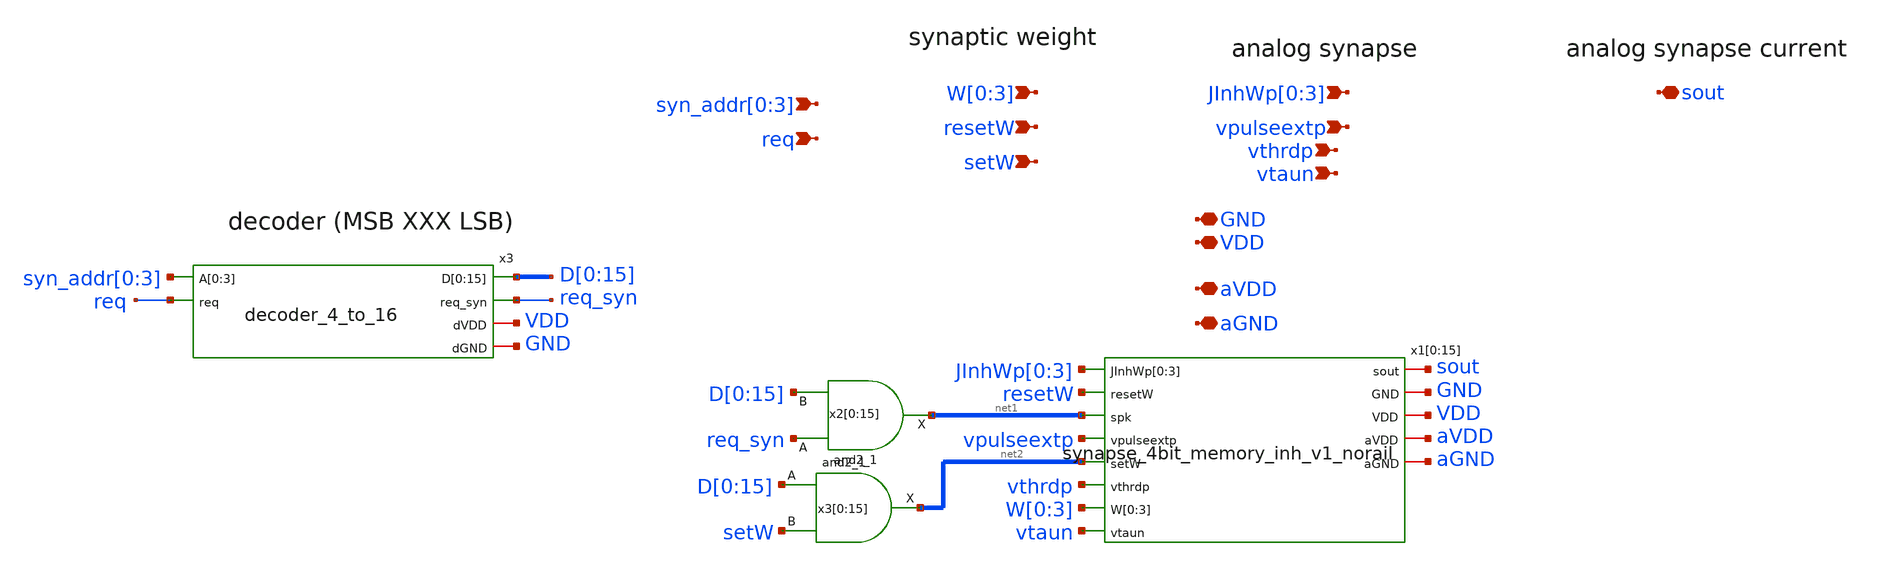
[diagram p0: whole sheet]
** sch_path: design/xschem/synapse_array_programmable_inh_16_to_sout_v1.sch
**.subckt synapse_array_programmable_inh_16_to_sout_v1 vpulseextp
*+ syn_addr[0],syn_addr[1],syn_addr[2],syn_addr[3] W[0],W[1],W[2],W[3] JInhWp[0],JInhWp[1],JInhWp[2],JInhWp[3] sout setW resetW req vthrdp vtaun GND
*+ VDD aVDD aGND
*.ipin vpulseextp
*.ipin syn_addr[0],syn_addr[1],syn_addr[2],syn_addr[3]
*.ipin W[0],W[1],W[2],W[3]
*.ipin JInhWp[0],JInhWp[1],JInhWp[2],JInhWp[3]
*.iopin sout
*.ipin setW
*.ipin resetW
*.ipin req
*.ipin vthrdp
*.ipin vtaun
*.iopin GND
*.iopin VDD
*.iopin aVDD
*.iopin aGND
x3 syn_addr[0] syn_addr[1] syn_addr[2] syn_addr[3] D[0] D[1] D[2] D[3] D[4] D[5] D[6] D[7] D[8] D[9]
+ D[10] D[11] D[12] D[13] D[14] D[15] req req_syn VDD GND decoder_4_to_16
x2[0] req_syn D[0] GND GND VDD VDD net1[15] sky130_fd_sc_hd__and2_1
x2[1] req_syn D[1] GND GND VDD VDD net1[14] sky130_fd_sc_hd__and2_1
x2[2] req_syn D[2] GND GND VDD VDD net1[13] sky130_fd_sc_hd__and2_1
x2[3] req_syn D[3] GND GND VDD VDD net1[12] sky130_fd_sc_hd__and2_1
x2[4] req_syn D[4] GND GND VDD VDD net1[11] sky130_fd_sc_hd__and2_1
x2[5] req_syn D[5] GND GND VDD VDD net1[10] sky130_fd_sc_hd__and2_1
x2[6] req_syn D[6] GND GND VDD VDD net1[9] sky130_fd_sc_hd__and2_1
x2[7] req_syn D[7] GND GND VDD VDD net1[8] sky130_fd_sc_hd__and2_1
x2[8] req_syn D[8] GND GND VDD VDD net1[7] sky130_fd_sc_hd__and2_1
x2[9] req_syn D[9] GND GND VDD VDD net1[6] sky130_fd_sc_hd__and2_1
x2[10] req_syn D[10] GND GND VDD VDD net1[5] sky130_fd_sc_hd__and2_1
x2[11] req_syn D[11] GND GND VDD VDD net1[4] sky130_fd_sc_hd__and2_1
x2[12] req_syn D[12] GND GND VDD VDD net1[3] sky130_fd_sc_hd__and2_1
x2[13] req_syn D[13] GND GND VDD VDD net1[2] sky130_fd_sc_hd__and2_1
x2[14] req_syn D[14] GND GND VDD VDD net1[1] sky130_fd_sc_hd__and2_1
x2[15] req_syn D[15] GND GND VDD VDD net1[0] sky130_fd_sc_hd__and2_1
x3[0] D[0] setW GND GND VDD VDD net2[15] sky130_fd_sc_hd__and2_1
x3[1] D[1] setW GND GND VDD VDD net2[14] sky130_fd_sc_hd__and2_1
x3[2] D[2] setW GND GND VDD VDD net2[13] sky130_fd_sc_hd__and2_1
x3[3] D[3] setW GND GND VDD VDD net2[12] sky130_fd_sc_hd__and2_1
x3[4] D[4] setW GND GND VDD VDD net2[11] sky130_fd_sc_hd__and2_1
x3[5] D[5] setW GND GND VDD VDD net2[10] sky130_fd_sc_hd__and2_1
x3[6] D[6] setW GND GND VDD VDD net2[9] sky130_fd_sc_hd__and2_1
x3[7] D[7] setW GND GND VDD VDD net2[8] sky130_fd_sc_hd__and2_1
x3[8] D[8] setW GND GND VDD VDD net2[7] sky130_fd_sc_hd__and2_1
x3[9] D[9] setW GND GND VDD VDD net2[6] sky130_fd_sc_hd__and2_1
x3[10] D[10] setW GND GND VDD VDD net2[5] sky130_fd_sc_hd__and2_1
x3[11] D[11] setW GND GND VDD VDD net2[4] sky130_fd_sc_hd__and2_1
x3[12] D[12] setW GND GND VDD VDD net2[3] sky130_fd_sc_hd__and2_1
x3[13] D[13] setW GND GND VDD VDD net2[2] sky130_fd_sc_hd__and2_1
x3[14] D[14] setW GND GND VDD VDD net2[1] sky130_fd_sc_hd__and2_1
x3[15] D[15] setW GND GND VDD VDD net2[0] sky130_fd_sc_hd__and2_1
x1[0] sout JInhWp[0] JInhWp[1] JInhWp[2] JInhWp[3] resetW net1[15] vpulseextp net2[15] vthrdp W[0]
+ W[1] W[2] W[3] vtaun GND VDD aVDD aGND synapse_4bit_memory_inh_v1_norail
x1[1] sout JInhWp[0] JInhWp[1] JInhWp[2] JInhWp[3] resetW net1[14] vpulseextp net2[14] vthrdp W[0]
+ W[1] W[2] W[3] vtaun GND VDD aVDD aGND synapse_4bit_memory_inh_v1_norail
x1[2] sout JInhWp[0] JInhWp[1] JInhWp[2] JInhWp[3] resetW net1[13] vpulseextp net2[13] vthrdp W[0]
+ W[1] W[2] W[3] vtaun GND VDD aVDD aGND synapse_4bit_memory_inh_v1_norail
x1[3] sout JInhWp[0] JInhWp[1] JInhWp[2] JInhWp[3] resetW net1[12] vpulseextp net2[12] vthrdp W[0]
+ W[1] W[2] W[3] vtaun GND VDD aVDD aGND synapse_4bit_memory_inh_v1_norail
x1[4] sout JInhWp[0] JInhWp[1] JInhWp[2] JInhWp[3] resetW net1[11] vpulseextp net2[11] vthrdp W[0]
+ W[1] W[2] W[3] vtaun GND VDD aVDD aGND synapse_4bit_memory_inh_v1_norail
x1[5] sout JInhWp[0] JInhWp[1] JInhWp[2] JInhWp[3] resetW net1[10] vpulseextp net2[10] vthrdp W[0]
+ W[1] W[2] W[3] vtaun GND VDD aVDD aGND synapse_4bit_memory_inh_v1_norail
x1[6] sout JInhWp[0] JInhWp[1] JInhWp[2] JInhWp[3] resetW net1[9] vpulseextp net2[9] vthrdp W[0]
+ W[1] W[2] W[3] vtaun GND VDD aVDD aGND synapse_4bit_memory_inh_v1_norail
x1[7] sout JInhWp[0] JInhWp[1] JInhWp[2] JInhWp[3] resetW net1[8] vpulseextp net2[8] vthrdp W[0]
+ W[1] W[2] W[3] vtaun GND VDD aVDD aGND synapse_4bit_memory_inh_v1_norail
x1[8] sout JInhWp[0] JInhWp[1] JInhWp[2] JInhWp[3] resetW net1[7] vpulseextp net2[7] vthrdp W[0]
+ W[1] W[2] W[3] vtaun GND VDD aVDD aGND synapse_4bit_memory_inh_v1_norail
x1[9] sout JInhWp[0] JInhWp[1] JInhWp[2] JInhWp[3] resetW net1[6] vpulseextp net2[6] vthrdp W[0]
+ W[1] W[2] W[3] vtaun GND VDD aVDD aGND synapse_4bit_memory_inh_v1_norail
x1[10] sout JInhWp[0] JInhWp[1] JInhWp[2] JInhWp[3] resetW net1[5] vpulseextp net2[5] vthrdp W[0]
+ W[1] W[2] W[3] vtaun GND VDD aVDD aGND synapse_4bit_memory_inh_v1_norail
x1[11] sout JInhWp[0] JInhWp[1] JInhWp[2] JInhWp[3] resetW net1[4] vpulseextp net2[4] vthrdp W[0]
+ W[1] W[2] W[3] vtaun GND VDD aVDD aGND synapse_4bit_memory_inh_v1_norail
x1[12] sout JInhWp[0] JInhWp[1] JInhWp[2] JInhWp[3] resetW net1[3] vpulseextp net2[3] vthrdp W[0]
+ W[1] W[2] W[3] vtaun GND VDD aVDD aGND synapse_4bit_memory_inh_v1_norail
x1[13] sout JInhWp[0] JInhWp[1] JInhWp[2] JInhWp[3] resetW net1[2] vpulseextp net2[2] vthrdp W[0]
+ W[1] W[2] W[3] vtaun GND VDD aVDD aGND synapse_4bit_memory_inh_v1_norail
x1[14] sout JInhWp[0] JInhWp[1] JInhWp[2] JInhWp[3] resetW net1[1] vpulseextp net2[1] vthrdp W[0]
+ W[1] W[2] W[3] vtaun GND VDD aVDD aGND synapse_4bit_memory_inh_v1_norail
x1[15] sout JInhWp[0] JInhWp[1] JInhWp[2] JInhWp[3] resetW net1[0] vpulseextp net2[0] vthrdp W[0]
+ W[1] W[2] W[3] vtaun GND VDD aVDD aGND synapse_4bit_memory_inh_v1_norail
**.ends

* expanding   symbol:  decoder_4_to_16.sym # of pins=6
** sym_path: design/xschem/decoder_4_to_16.sym
** sch_path: design/xschem/decoder_4_to_16.sch
.subckt decoder_4_to_16 A[0] A[1] A[2] A[3] D[0] D[1] D[2] D[3] D[4] D[5] D[6] D[7] D[8] D[9] D[10]
+ D[11] D[12] D[13] D[14] D[15] req req_syn dVDD dGND
*.ipin A[0],A[1],A[2],A[3]
*.ipin req
*.opin D[0],D[1],D[2],D[3],D[4],D[5],D[6],D[7],D[8],D[9],D[10],D[11],D[12],D[13],D[14],D[15]
*.opin req_syn
*.iopin dVDD
*.iopin dGND
x21 req dGND dGND dVDD dVDD net5 sky130_fd_sc_hd__inv_1
x22 net5 dGND dGND dVDD dVDD net6 sky130_fd_sc_hd__inv_1
x23 net6 dGND dGND dVDD dVDD net7 sky130_fd_sc_hd__inv_1
x24 net7 dGND dGND dVDD dVDD req_syn sky130_fd_sc_hd__inv_1
x20 A[3] A[2] A[1] A[0] dGND dGND dVDD dVDD D[15] sky130_fd_sc_hd__and4_1
x19 A[3] A[2] A[1] net4 dGND dGND dVDD dVDD D[14] sky130_fd_sc_hd__and4_1
x18 A[3] A[2] net3 A[0] dGND dGND dVDD dVDD D[13] sky130_fd_sc_hd__and4_1
x17 A[3] A[2] net3 net4 dGND dGND dVDD dVDD D[12] sky130_fd_sc_hd__and4_1
x16 A[3] net2 A[1] A[0] dGND dGND dVDD dVDD D[11] sky130_fd_sc_hd__and4_1
x15 A[3] net2 A[1] net4 dGND dGND dVDD dVDD D[10] sky130_fd_sc_hd__and4_1
x13 A[3] net2 net3 A[0] dGND dGND dVDD dVDD D[9] sky130_fd_sc_hd__and4_1
x4 A[3] net2 net3 net4 dGND dGND dVDD dVDD D[8] sky130_fd_sc_hd__and4_1
x5 net1 A[2] A[1] A[0] dGND dGND dVDD dVDD D[7] sky130_fd_sc_hd__and4_1
x6 net1 A[2] A[1] net4 dGND dGND dVDD dVDD D[6] sky130_fd_sc_hd__and4_1
x8 net1 A[2] net3 net4 dGND dGND dVDD dVDD D[4] sky130_fd_sc_hd__and4_1
x9 net1 net2 A[1] net4 dGND dGND dVDD dVDD D[2] sky130_fd_sc_hd__and4_1
x10 net1 net2 net3 net4 dGND dGND dVDD dVDD D[0] sky130_fd_sc_hd__and4_1
x11 net1 net2 net3 A[0] dGND dGND dVDD dVDD D[1] sky130_fd_sc_hd__and4_1
x12 net1 net2 A[1] A[0] dGND dGND dVDD dVDD D[3] sky130_fd_sc_hd__and4_1
x14 net1 A[2] net3 A[0] dGND dGND dVDD dVDD D[5] sky130_fd_sc_hd__and4_1
x1 A[3] dGND dGND dVDD dVDD net1 sky130_fd_sc_hd__inv_4
x2 A[2] dGND dGND dVDD dVDD net2 sky130_fd_sc_hd__inv_4
x3 A[1] dGND dGND dVDD dVDD net3 sky130_fd_sc_hd__inv_4
x7 A[0] dGND dGND dVDD dVDD net4 sky130_fd_sc_hd__inv_4
.ends


* expanding   symbol:  synapse_4bit_memory_inh_v1_norail.sym # of pins=13
** sym_path: design/xschem/synapse_4bit_memory_inh_v1_norail.sym
** sch_path: design/xschem/synapse_4bit_memory_inh_v1_norail.sch
.subckt synapse_4bit_memory_inh_v1_norail sout JInhWp[0] JInhWp[1] JInhWp[2] JInhWp[3] resetW spk
+ vpulseextp setW vthrdp W[0] W[1] W[2] W[3] vtaun GND VDD aVDD aGND
*.ipin vpulseextp
*.ipin spk
*.ipin JInhWp[0],JInhWp[1],JInhWp[2],JInhWp[3]
*.ipin W[0],W[1],W[2],W[3]
*.ipin setW
*.ipin resetW
*.iopin sout
*.ipin vthrdp
*.ipin vtaun
*.iopin GND
*.iopin VDD
*.iopin aVDD
*.iopin aGND
x11 resetW GND GND VDD VDD net1 sky130_fd_sc_hd__inv_1
x2 JInhWp[0] JInhWp[1] JInhWp[2] JInhWp[3] net2[3] net2[2] net2[1] net2[0] spke sout vthrdp vtaun
+ aGND aVDD dpi_syn_inh_4bit_fc_v2
x2[0] setW W[0] net1 GND GND VDD VDD net3[3] net2[3] sky130_fd_sc_hd__dfrbp_1
x2[1] setW W[1] net1 GND GND VDD VDD net3[2] net2[2] sky130_fd_sc_hd__dfrbp_1
x2[2] setW W[2] net1 GND GND VDD VDD net3[1] net2[1] sky130_fd_sc_hd__dfrbp_1
x2[3] setW W[3] net1 GND GND VDD VDD net3[0] net2[0] sky130_fd_sc_hd__dfrbp_1
x4 vpulseextp spk GND spke VDD spike_extender_with_trimming
x1 GND GND VDD VDD sky130_fd_sc_hd__decap_4
.ends


* expanding   symbol:  dpi_syn_inh_4bit_fc_v2.sym # of pins=8
** sym_path: design/xschem/dpi_syn_inh_4bit_fc_v2.sym
** sch_path: design/xschem/dpi_syn_inh_4bit_fc_v2.sch
.subckt dpi_syn_inh_4bit_fc_v2 JInhWp[0] JInhWp[1] JInhWp[2] JInhWp[3] weight_b[0] weight_b[1]
+ weight_b[2] weight_b[3] spk sout vthrdp vtaun GND aVDD
*.ipin spk
*.iopin vthrdp
*.iopin vtaun
*.iopin sout
*.iopin GND
*.iopin aVDD
*.ipin weight_b[0],weight_b[1],weight_b[2],weight_b[3]
*.iopin JInhWp[0],JInhWp[1],JInhWp[2],JInhWp[3]
XM5 net2 net3 net1 aVDD sky130_fd_pr__pfet_01v8 L=0.2 W=1.2 nf=1 ad='int((nf+1)/2) * W/nf * 0.29' as='int((nf+2)/2) * W/nf * 0.29'
+ pd='2*int((nf+1)/2) * (W/nf + 0.29)' ps='2*int((nf+2)/2) * (W/nf + 0.29)' nrd='0.29 / W' nrs='0.29 / W'
+ sa=0 sb=0 sd=0 mult=1 m=1
XM2 GND vthrdp net2 aVDD sky130_fd_pr__pfet_01v8 L=0.2 W=1.2 nf=1 ad='int((nf+1)/2) * W/nf * 0.29' as='int((nf+2)/2) * W/nf * 0.29'
+ pd='2*int((nf+1)/2) * (W/nf + 0.29)' ps='2*int((nf+2)/2) * (W/nf + 0.29)' nrd='0.29 / W' nrs='0.29 / W'
+ sa=0 sb=0 sd=0 mult=1 m=1
XM3 vsin vsin net2 aVDD sky130_fd_pr__pfet_01v8 L=0.2 W=1.2 nf=1 ad='int((nf+1)/2) * W/nf * 0.29' as='int((nf+2)/2) * W/nf * 0.29'
+ pd='2*int((nf+1)/2) * (W/nf + 0.29)' ps='2*int((nf+2)/2) * (W/nf + 0.29)' nrd='0.29 / W' nrs='0.29 / W'
+ sa=0 sb=0 sd=0 mult=1 m=1
XM4 vsin vtaun GND GND sky130_fd_pr__nfet_01v8 L=0.25 W=1.0 nf=1 ad='int((nf+1)/2) * W/nf * 0.29' as='int((nf+2)/2) * W/nf * 0.29'
+ pd='2*int((nf+1)/2) * (W/nf + 0.29)' ps='2*int((nf+2)/2) * (W/nf + 0.29)' nrd='0.29 / W' nrs='0.29 / W'
+ sa=0 sb=0 sd=0 mult=1 m=1
XM6 sout vsin GND GND sky130_fd_pr__nfet_01v8 L=0.25 W=1.0 nf=1 ad='int((nf+1)/2) * W/nf * 0.29' as='int((nf+2)/2) * W/nf * 0.29'
+ pd='2*int((nf+1)/2) * (W/nf + 0.29)' ps='2*int((nf+2)/2) * (W/nf + 0.29)' nrd='0.29 / W' nrs='0.29 / W'
+ sa=0 sb=0 sd=0 mult=1 m=1
XM7 net3 spk GND GND sky130_fd_pr__nfet_01v8 L=0.25 W=1.0 nf=1 ad='int((nf+1)/2) * W/nf * 0.29' as='int((nf+2)/2) * W/nf * 0.29'
+ pd='2*int((nf+1)/2) * (W/nf + 0.29)' ps='2*int((nf+2)/2) * (W/nf + 0.29)' nrd='0.29 / W' nrs='0.29 / W'
+ sa=0 sb=0 sd=0 mult=1 m=1
XM8 net3 spk aVDD aVDD sky130_fd_pr__pfet_01v8 L=0.2 W=1.2 nf=1 ad='int((nf+1)/2) * W/nf * 0.29' as='int((nf+2)/2) * W/nf * 0.29'
+ pd='2*int((nf+1)/2) * (W/nf + 0.29)' ps='2*int((nf+2)/2) * (W/nf + 0.29)' nrd='0.29 / W' nrs='0.29 / W'
+ sa=0 sb=0 sd=0 mult=1 m=1
XC1 vsin GND sky130_fd_pr__cap_mim_m3_1 W=5 L=5 MF=1 m=1
XM9 net4 JInhWp[0] aVDD aVDD sky130_fd_pr__pfet_01v8 L=1.2 W=1.2 nf=1 ad='int((nf+1)/2) * W/nf * 0.29'
+ as='int((nf+2)/2) * W/nf * 0.29' pd='2*int((nf+1)/2) * (W/nf + 0.29)' ps='2*int((nf+2)/2) * (W/nf + 0.29)'
+ nrd='0.29 / W' nrs='0.29 / W' sa=0 sb=0 sd=0 mult=1 m=1
XM10 net1 weight_b[0] net4 aVDD sky130_fd_pr__pfet_01v8 L=0.2 W=1.2 nf=1 ad='int((nf+1)/2) * W/nf * 0.29'
+ as='int((nf+2)/2) * W/nf * 0.29' pd='2*int((nf+1)/2) * (W/nf + 0.29)' ps='2*int((nf+2)/2) * (W/nf + 0.29)'
+ nrd='0.29 / W' nrs='0.29 / W' sa=0 sb=0 sd=0 mult=1 m=1
XM11 net1 weight_b[1] net5 aVDD sky130_fd_pr__pfet_01v8 L=0.2 W=1.2 nf=1 ad='int((nf+1)/2) * W/nf * 0.29'
+ as='int((nf+2)/2) * W/nf * 0.29' pd='2*int((nf+1)/2) * (W/nf + 0.29)' ps='2*int((nf+2)/2) * (W/nf + 0.29)'
+ nrd='0.29 / W' nrs='0.29 / W' sa=0 sb=0 sd=0 mult=1 m=1
XM1 net5 JInhWp[1] aVDD aVDD sky130_fd_pr__pfet_01v8 L=2.0 W=1.2 nf=1 ad='int((nf+1)/2) * W/nf * 0.29'
+ as='int((nf+2)/2) * W/nf * 0.29' pd='2*int((nf+1)/2) * (W/nf + 0.29)' ps='2*int((nf+2)/2) * (W/nf + 0.29)'
+ nrd='0.29 / W' nrs='0.29 / W' sa=0 sb=0 sd=0 mult=1 m=1
XM12 net6 JInhWp[2] aVDD aVDD sky130_fd_pr__pfet_01v8 L=4.0 W=1.2 nf=1 ad='int((nf+1)/2) * W/nf * 0.29'
+ as='int((nf+2)/2) * W/nf * 0.29' pd='2*int((nf+1)/2) * (W/nf + 0.29)' ps='2*int((nf+2)/2) * (W/nf + 0.29)'
+ nrd='0.29 / W' nrs='0.29 / W' sa=0 sb=0 sd=0 mult=1 m=1
XM13 net7 JInhWp[3] aVDD aVDD sky130_fd_pr__pfet_01v8 L=8.0 W=1.2 nf=1 ad='int((nf+1)/2) * W/nf * 0.29'
+ as='int((nf+2)/2) * W/nf * 0.29' pd='2*int((nf+1)/2) * (W/nf + 0.29)' ps='2*int((nf+2)/2) * (W/nf + 0.29)'
+ nrd='0.29 / W' nrs='0.29 / W' sa=0 sb=0 sd=0 mult=1 m=1
XM14 net1 weight_b[2] net6 aVDD sky130_fd_pr__pfet_01v8 L=0.2 W=1.2 nf=1 ad='int((nf+1)/2) * W/nf * 0.29'
+ as='int((nf+2)/2) * W/nf * 0.29' pd='2*int((nf+1)/2) * (W/nf + 0.29)' ps='2*int((nf+2)/2) * (W/nf + 0.29)'
+ nrd='0.29 / W' nrs='0.29 / W' sa=0 sb=0 sd=0 mult=1 m=1
XM15 net1 weight_b[3] net7 aVDD sky130_fd_pr__pfet_01v8 L=0.2 W=1.2 nf=1 ad='int((nf+1)/2) * W/nf * 0.29'
+ as='int((nf+2)/2) * W/nf * 0.29' pd='2*int((nf+1)/2) * (W/nf + 0.29)' ps='2*int((nf+2)/2) * (W/nf + 0.29)'
+ nrd='0.29 / W' nrs='0.29 / W' sa=0 sb=0 sd=0 mult=1 m=1
.ends


* expanding   symbol:  spike_extender_with_trimming.sym # of pins=5
** sym_path: design/xschem/spike_extender_with_trimming.sym
** sch_path: design/xschem/spike_extender_with_trimming.sch
.subckt spike_extender_with_trimming vpulseextp vspk GND spkext VDD
*.iopin GND
*.iopin VDD
*.ipin vspk
*.opin spkext
*.ipin vpulseextp
x1 vpulseextp vpulseshort GND spkext VDD spike_extender
x3 vspk GND GND VDD VDD net1 sky130_fd_sc_hd__clkdlybuf4s50_1
x2 net1 vspk GND GND VDD VDD vpulseshort sky130_fd_sc_hd__nor2b_1
.ends


* expanding   symbol:  spike_extender.sym # of pins=5
** sym_path: design/xschem/spike_extender.sym
** sch_path: design/xschem/spike_extender.sch
.subckt spike_extender vpulseextp spk GND spkext VDD
*.iopin GND
*.iopin VDD
*.ipin spk
*.opin spkext
*.ipin vpulseextp
XM1 net1 spk GND GND sky130_fd_pr__nfet_01v8 L=0.15 W=0.65 nf=1 ad='int((nf+1)/2) * W/nf * 0.29' as='int((nf+2)/2) * W/nf * 0.29'
+ pd='2*int((nf+1)/2) * (W/nf + 0.29)' ps='2*int((nf+2)/2) * (W/nf + 0.29)' nrd='0.29 / W' nrs='0.29 / W'
+ sa=0 sb=0 sd=0 mult=1 m=1
XM6 net1 vpulseextp VDD VDD sky130_fd_pr__pfet_01v8 L=2 W=1 nf=1 ad='int((nf+1)/2) * W/nf * 0.29' as='int((nf+2)/2) * W/nf * 0.29'
+ pd='2*int((nf+1)/2) * (W/nf + 0.29)' ps='2*int((nf+2)/2) * (W/nf + 0.29)' nrd='0.29 / W' nrs='0.29 / W'
+ sa=0 sb=0 sd=0 mult=1 m=1
XM5 net3 net2 GND GND sky130_fd_pr__nfet_01v8 L=0.15 W=0.65 nf=1 ad='int((nf+1)/2) * W/nf * 0.29' as='int((nf+2)/2) * W/nf * 0.29'
+ pd='2*int((nf+1)/2) * (W/nf + 0.29)' ps='2*int((nf+2)/2) * (W/nf + 0.29)' nrd='0.29 / W' nrs='0.29 / W'
+ sa=0 sb=0 sd=0 mult=1 m=1
XM8 spkext net3 GND GND sky130_fd_pr__nfet_01v8 L=0.15 W=0.65 nf=1 ad='int((nf+1)/2) * W/nf * 0.29' as='int((nf+2)/2) * W/nf * 0.29'
+ pd='2*int((nf+1)/2) * (W/nf + 0.29)' ps='2*int((nf+2)/2) * (W/nf + 0.29)' nrd='0.29 / W' nrs='0.29 / W'
+ sa=0 sb=0 sd=0 mult=1 m=1
XM4 net3 net2 VDD VDD sky130_fd_pr__pfet_01v8 L=0.15 W=1.0 nf=1 ad='int((nf+1)/2) * W/nf * 0.29' as='int((nf+2)/2) * W/nf * 0.29'
+ pd='2*int((nf+1)/2) * (W/nf + 0.29)' ps='2*int((nf+2)/2) * (W/nf + 0.29)' nrd='0.29 / W' nrs='0.29 / W'
+ sa=0 sb=0 sd=0 mult=1 m=1
XM7 spkext net3 VDD VDD sky130_fd_pr__pfet_01v8 L=0.15 W=1.0 nf=1 ad='int((nf+1)/2) * W/nf * 0.29' as='int((nf+2)/2) * W/nf * 0.29'
+ pd='2*int((nf+1)/2) * (W/nf + 0.29)' ps='2*int((nf+2)/2) * (W/nf + 0.29)' nrd='0.29 / W' nrs='0.29 / W'
+ sa=0 sb=0 sd=0 mult=1 m=1
XM2 net2 net1 GND GND sky130_fd_pr__nfet_01v8 L=0.15 W=0.65 nf=1 ad='int((nf+1)/2) * W/nf * 0.29' as='int((nf+2)/2) * W/nf * 0.29'
+ pd='2*int((nf+1)/2) * (W/nf + 0.29)' ps='2*int((nf+2)/2) * (W/nf + 0.29)' nrd='0.29 / W' nrs='0.29 / W'
+ sa=0 sb=0 sd=0 mult=1 m=1
XM3 net2 net1 VDD VDD sky130_fd_pr__pfet_01v8 L=0.15 W=1.0 nf=1 ad='int((nf+1)/2) * W/nf * 0.29' as='int((nf+2)/2) * W/nf * 0.29'
+ pd='2*int((nf+1)/2) * (W/nf + 0.29)' ps='2*int((nf+2)/2) * (W/nf + 0.29)' nrd='0.29 / W' nrs='0.29 / W'
+ sa=0 sb=0 sd=0 mult=1 m=1
XM9 GND net1 GND GND sky130_fd_pr__nfet_01v8 L=1 W=0.65 nf=1 ad='int((nf+1)/2) * W/nf * 0.29' as='int((nf+2)/2) * W/nf * 0.29'
+ pd='2*int((nf+1)/2) * (W/nf + 0.29)' ps='2*int((nf+2)/2) * (W/nf + 0.29)' nrd='0.29 / W' nrs='0.29 / W'
+ sa=0 sb=0 sd=0 mult=1 m=1
.ends

.end
